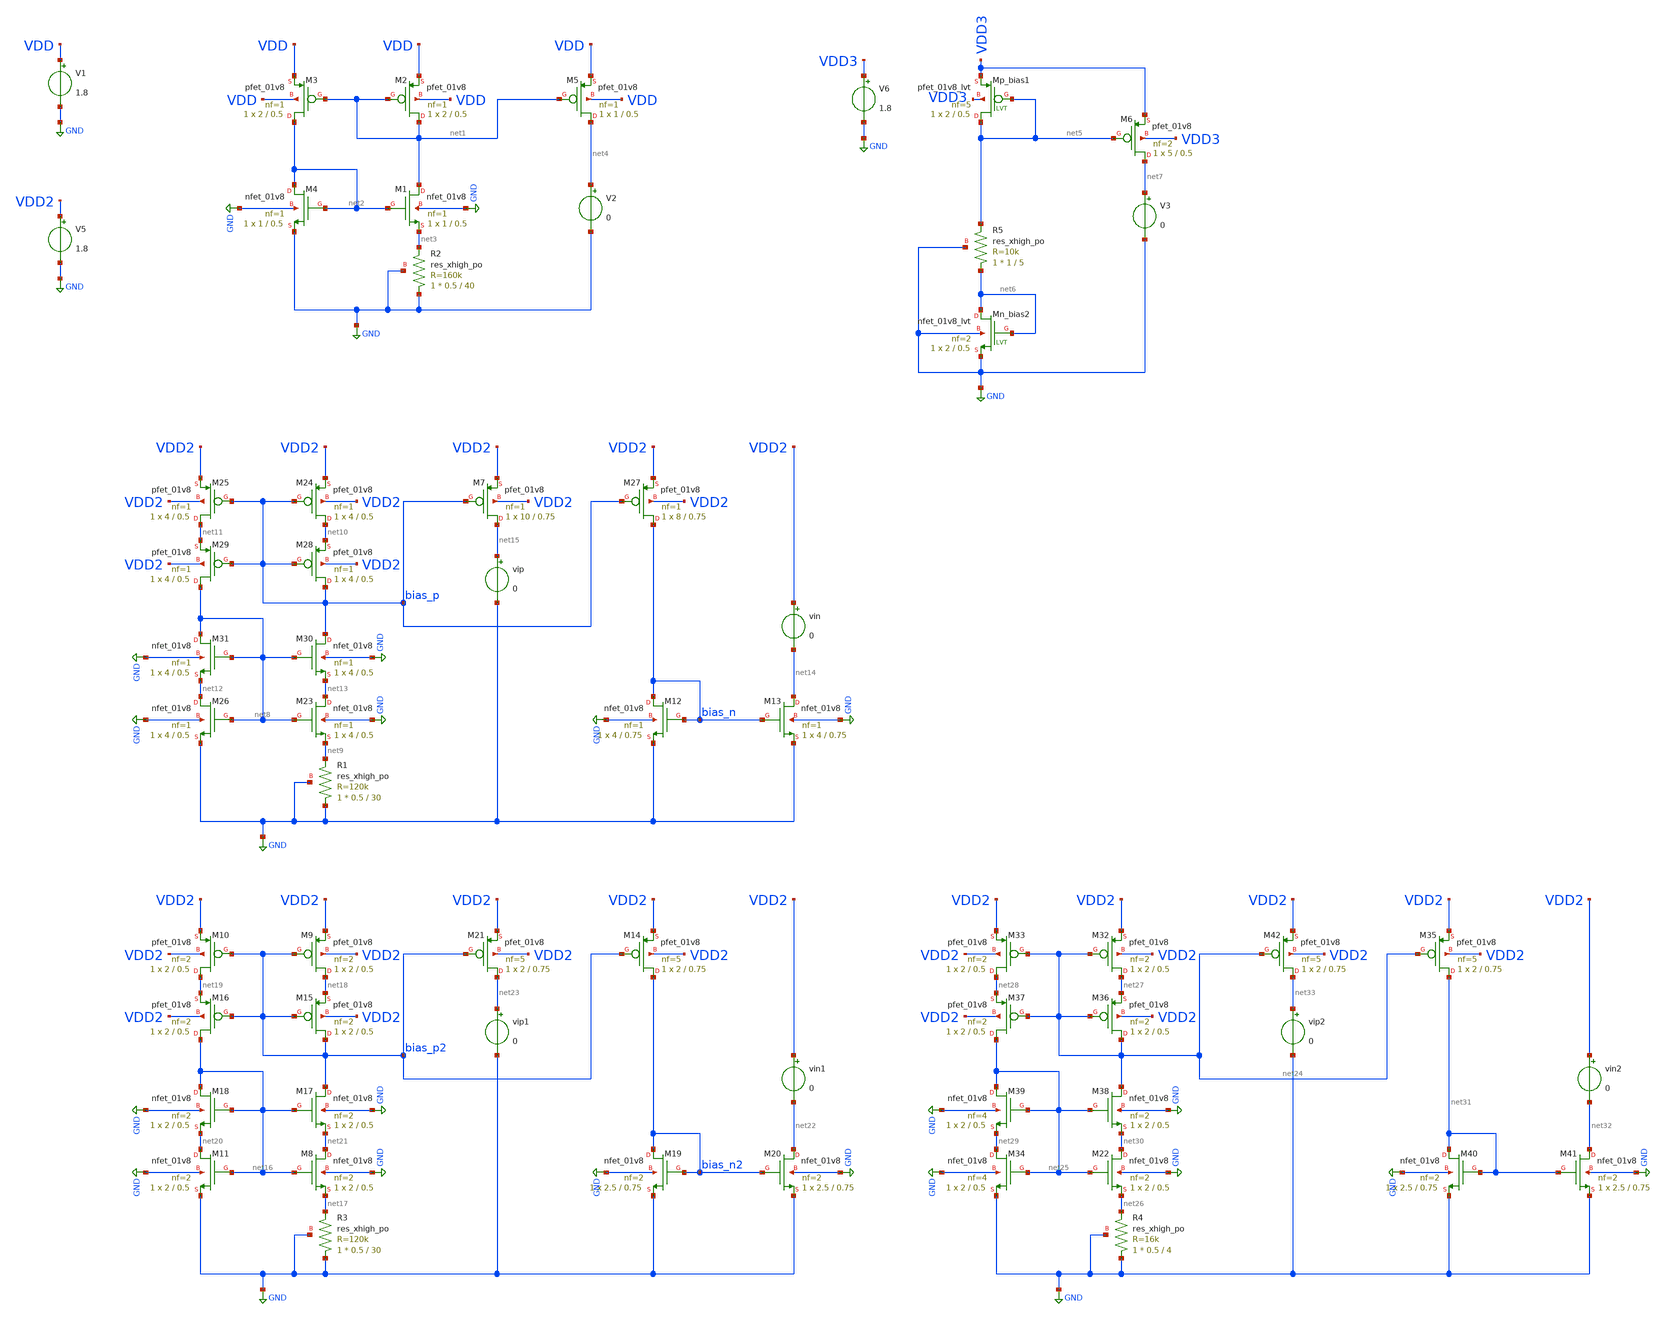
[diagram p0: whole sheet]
** sch_path: schem/ptat_isource.sch
**.subckt ptat_isource
XM1 net1 net2 net3 GND sky130_fd_pr__nfet_01v8 L=0.5 W=1 nf=1 ad='int((1 + 1)/2) * 1 / 1 * 0.29' as='int((1 + 2)/2) * 1 / 1 * 0.29'
+ pd='2*int((1 + 1)/2) * (1 / 1 + 0.29)' ps='2*int((1 + 2)/2) * (1 / 1 + 0.29)' nrd='0.29 / 1 ' nrs='0.29 / 1 '
+ sa=0 sb=0 sd=0 mult=1 m=1
XM2 net1 net1 VDD VDD sky130_fd_pr__pfet_01v8 L=0.5 W=2 nf=1 ad='int((1 + 1)/2) * 2 / 1 * 0.29' as='int((1 + 2)/2) * 2 / 1 * 0.29'
+ pd='2*int((1 + 1)/2) * (2 / 1 + 0.29)' ps='2*int((1 + 2)/2) * (2 / 1 + 0.29)' nrd='0.29 / 2 ' nrs='0.29 / 2 '
+ sa=0 sb=0 sd=0 mult=1 m=1
XM3 net2 net1 VDD VDD sky130_fd_pr__pfet_01v8 L=0.5 W=2 nf=1 ad='int((1 + 1)/2) * 2 / 1 * 0.29' as='int((1 + 2)/2) * 2 / 1 * 0.29'
+ pd='2*int((1 + 1)/2) * (2 / 1 + 0.29)' ps='2*int((1 + 2)/2) * (2 / 1 + 0.29)' nrd='0.29 / 2 ' nrs='0.29 / 2 '
+ sa=0 sb=0 sd=0 mult=1 m=1
XM4 net2 net2 GND GND sky130_fd_pr__nfet_01v8 L=0.5 W=1 nf=1 ad='int((1 + 1)/2) * 1 / 1 * 0.29' as='int((1 + 2)/2) * 1 / 1 * 0.29'
+ pd='2*int((1 + 1)/2) * (1 / 1 + 0.29)' ps='2*int((1 + 2)/2) * (1 / 1 + 0.29)' nrd='0.29 / 1 ' nrs='0.29 / 1 '
+ sa=0 sb=0 sd=0 mult=1 m=1
XR2 GND net3 GND sky130_fd_pr__res_xhigh_po W=0.5 L=40 mult=1 m=1
V1 VDD GND 1.8
XM5 net4 net1 VDD VDD sky130_fd_pr__pfet_01v8 L=0.5 W=1 nf=1 ad='int((1 + 1)/2) * 1 / 1 * 0.29' as='int((1 + 2)/2) * 1 / 1 * 0.29'
+ pd='2*int((1 + 1)/2) * (1 / 1 + 0.29)' ps='2*int((1 + 2)/2) * (1 / 1 + 0.29)' nrd='0.29 / 1 ' nrs='0.29 / 1 '
+ sa=0 sb=0 sd=0 mult=1 m=1
V2 net4 GND 0
XM6 net7 net5 VDD3 VDD3 sky130_fd_pr__pfet_01v8 L=0.5 W=5 nf=2 ad='int((2 + 1)/2) * 5 / 2 * 0.29' as='int((2 + 2)/2) * 5 / 2 * 0.29'
+ pd='2*int((2 + 1)/2) * (5 / 2 + 0.29)' ps='2*int((2 + 2)/2) * (5 / 2 + 0.29)' nrd='0.29 / 5 ' nrs='0.29 / 5 '
+ sa=0 sb=0 sd=0 mult=1 m=1
V3 net7 GND 0
XMn_bias2 net6 net6 GND GND sky130_fd_pr__nfet_01v8_lvt L=0.5 W=2 nf=2 ad='int((nf+1)/2) * W/nf * 0.29'
+ as='int((nf+2)/2) * W/nf * 0.29' pd='2*int((nf+1)/2) * (W/nf + 0.29)' ps='2*int((nf+2)/2) * (W/nf + 0.29)'
+ nrd='0.29 / W' nrs='0.29 / W' sa=0 sb=0 sd=0 mult=1 m=1
XMp_bias1 net5 net5 VDD3 VDD3 sky130_fd_pr__pfet_01v8_lvt L=0.5 W=2 nf=5 ad='int((nf+1)/2) * W/nf * 0.29'
+ as='int((nf+2)/2) * W/nf * 0.29' pd='2*int((nf+1)/2) * (W/nf + 0.29)' ps='2*int((nf+2)/2) * (W/nf + 0.29)'
+ nrd='0.29 / W' nrs='0.29 / W' sa=0 sb=0 sd=0 mult=1 m=1
V5 VDD2 GND 1.8
V6 VDD3 GND 1.8
XM23 net13 net8 net9 GND sky130_fd_pr__nfet_01v8 L=0.5 W=4 nf=1 ad='int((1 + 1)/2) * 4 / 1 * 0.29' as='int((1 + 2)/2) * 4 / 1 * 0.29'
+ pd='2*int((1 + 1)/2) * (4 / 1 + 0.29)' ps='2*int((1 + 2)/2) * (4 / 1 + 0.29)' nrd='0.29 / 4 ' nrs='0.29 / 4 '
+ sa=0 sb=0 sd=0 mult=1 m=1
XM24 net10 bias_p VDD2 VDD2 sky130_fd_pr__pfet_01v8 L=0.5 W=4 nf=1 ad='int((1 + 1)/2) * 4 / 1 * 0.29'
+ as='int((1 + 2)/2) * 4 / 1 * 0.29' pd='2*int((1 + 1)/2) * (4 / 1 + 0.29)' ps='2*int((1 + 2)/2) * (4 / 1 + 0.29)'
+ nrd='0.29 / 4 ' nrs='0.29 / 4 ' sa=0 sb=0 sd=0 mult=1 m=1
XM25 net11 bias_p VDD2 VDD2 sky130_fd_pr__pfet_01v8 L=0.5 W=4 nf=1 ad='int((1 + 1)/2) * 4 / 1 * 0.29'
+ as='int((1 + 2)/2) * 4 / 1 * 0.29' pd='2*int((1 + 1)/2) * (4 / 1 + 0.29)' ps='2*int((1 + 2)/2) * (4 / 1 + 0.29)'
+ nrd='0.29 / 4 ' nrs='0.29 / 4 ' sa=0 sb=0 sd=0 mult=1 m=1
XM26 net12 net8 GND GND sky130_fd_pr__nfet_01v8 L=0.5 W=4 nf=1 ad='int((1 + 1)/2) * 4 / 1 * 0.29' as='int((1 + 2)/2) * 4 / 1 * 0.29'
+ pd='2*int((1 + 1)/2) * (4 / 1 + 0.29)' ps='2*int((1 + 2)/2) * (4 / 1 + 0.29)' nrd='0.29 / 4 ' nrs='0.29 / 4 '
+ sa=0 sb=0 sd=0 mult=1 m=1
XR1 GND net9 GND sky130_fd_pr__res_xhigh_po W=0.5 L=30 mult=1 m=1
XM27 bias_n bias_p VDD2 VDD2 sky130_fd_pr__pfet_01v8 L=0.75 W=8 nf=1 ad='int((1 + 1)/2) * 8 / 1 * 0.29'
+ as='int((1 + 2)/2) * 8 / 1 * 0.29' pd='2*int((1 + 1)/2) * (8 / 1 + 0.29)' ps='2*int((1 + 2)/2) * (8 / 1 + 0.29)'
+ nrd='0.29 / 8 ' nrs='0.29 / 8 ' sa=0 sb=0 sd=0 mult=1 m=1
XM28 bias_p bias_p net10 VDD2 sky130_fd_pr__pfet_01v8 L=0.5 W=4 nf=1 ad='int((1 + 1)/2) * 4 / 1 * 0.29'
+ as='int((1 + 2)/2) * 4 / 1 * 0.29' pd='2*int((1 + 1)/2) * (4 / 1 + 0.29)' ps='2*int((1 + 2)/2) * (4 / 1 + 0.29)'
+ nrd='0.29 / 4 ' nrs='0.29 / 4 ' sa=0 sb=0 sd=0 mult=1 m=1
XM29 net8 bias_p net11 VDD2 sky130_fd_pr__pfet_01v8 L=0.5 W=4 nf=1 ad='int((1 + 1)/2) * 4 / 1 * 0.29'
+ as='int((1 + 2)/2) * 4 / 1 * 0.29' pd='2*int((1 + 1)/2) * (4 / 1 + 0.29)' ps='2*int((1 + 2)/2) * (4 / 1 + 0.29)'
+ nrd='0.29 / 4 ' nrs='0.29 / 4 ' sa=0 sb=0 sd=0 mult=1 m=1
XM30 bias_p net8 net13 GND sky130_fd_pr__nfet_01v8 L=0.5 W=4 nf=1 ad='int((1 + 1)/2) * 4 / 1 * 0.29'
+ as='int((1 + 2)/2) * 4 / 1 * 0.29' pd='2*int((1 + 1)/2) * (4 / 1 + 0.29)' ps='2*int((1 + 2)/2) * (4 / 1 + 0.29)'
+ nrd='0.29 / 4 ' nrs='0.29 / 4 ' sa=0 sb=0 sd=0 mult=1 m=1
XM31 net8 net8 net12 GND sky130_fd_pr__nfet_01v8 L=0.5 W=4 nf=1 ad='int((1 + 1)/2) * 4 / 1 * 0.29' as='int((1 + 2)/2) * 4 / 1 * 0.29'
+ pd='2*int((1 + 1)/2) * (4 / 1 + 0.29)' ps='2*int((1 + 2)/2) * (4 / 1 + 0.29)' nrd='0.29 / 4 ' nrs='0.29 / 4 '
+ sa=0 sb=0 sd=0 mult=1 m=1
XM12 bias_n bias_n GND GND sky130_fd_pr__nfet_01v8 L=0.75 W=4 nf=1 ad='int((1 + 1)/2) * 4 / 1 * 0.29'
+ as='int((1 + 2)/2) * 4 / 1 * 0.29' pd='2*int((1 + 1)/2) * (4 / 1 + 0.29)' ps='2*int((1 + 2)/2) * (4 / 1 + 0.29)'
+ nrd='0.29 / 4 ' nrs='0.29 / 4 ' sa=0 sb=0 sd=0 mult=1 m=1
XM13 net14 bias_n GND GND sky130_fd_pr__nfet_01v8 L=0.75 W=4 nf=1 ad='int((1 + 1)/2) * 4 / 1 * 0.29'
+ as='int((1 + 2)/2) * 4 / 1 * 0.29' pd='2*int((1 + 1)/2) * (4 / 1 + 0.29)' ps='2*int((1 + 2)/2) * (4 / 1 + 0.29)'
+ nrd='0.29 / 4 ' nrs='0.29 / 4 ' sa=0 sb=0 sd=0 mult=1 m=1
vin VDD2 net14 0
XM7 net15 bias_p VDD2 VDD2 sky130_fd_pr__pfet_01v8 L=0.75 W=10 nf=1 ad='int((1 + 1)/2) * 10 / 1 * 0.29'
+ as='int((1 + 2)/2) * 10 / 1 * 0.29' pd='2*int((1 + 1)/2) * (10 / 1 + 0.29)' ps='2*int((1 + 2)/2) * (10 / 1 + 0.29)'
+ nrd='0.29 / 10 ' nrs='0.29 / 10 ' sa=0 sb=0 sd=0 mult=1 m=1
vip net15 GND 0
XM8 net21 net16 net17 GND sky130_fd_pr__nfet_01v8 L=0.5 W=2 nf=2 ad='int((2 + 1)/2) * 2 / 2 * 0.29' as='int((2 + 2)/2) * 2 / 2 * 0.29'
+ pd='2*int((2 + 1)/2) * (2 / 2 + 0.29)' ps='2*int((2 + 2)/2) * (2 / 2 + 0.29)' nrd='0.29 / 2 ' nrs='0.29 / 2 '
+ sa=0 sb=0 sd=0 mult=1 m=1
XM9 net18 bias_p2 VDD2 VDD2 sky130_fd_pr__pfet_01v8 L=0.5 W=2 nf=2 ad='int((2 + 1)/2) * 2 / 2 * 0.29'
+ as='int((2 + 2)/2) * 2 / 2 * 0.29' pd='2*int((2 + 1)/2) * (2 / 2 + 0.29)' ps='2*int((2 + 2)/2) * (2 / 2 + 0.29)'
+ nrd='0.29 / 2 ' nrs='0.29 / 2 ' sa=0 sb=0 sd=0 mult=1 m=1
XM10 net19 bias_p2 VDD2 VDD2 sky130_fd_pr__pfet_01v8 L=0.5 W=2 nf=2 ad='int((2 + 1)/2) * 2 / 2 * 0.29'
+ as='int((2 + 2)/2) * 2 / 2 * 0.29' pd='2*int((2 + 1)/2) * (2 / 2 + 0.29)' ps='2*int((2 + 2)/2) * (2 / 2 + 0.29)'
+ nrd='0.29 / 2 ' nrs='0.29 / 2 ' sa=0 sb=0 sd=0 mult=1 m=1
XM11 net20 net16 GND GND sky130_fd_pr__nfet_01v8 L=0.5 W=2 nf=2 ad='int((2 + 1)/2) * 2 / 2 * 0.29' as='int((2 + 2)/2) * 2 / 2 * 0.29'
+ pd='2*int((2 + 1)/2) * (2 / 2 + 0.29)' ps='2*int((2 + 2)/2) * (2 / 2 + 0.29)' nrd='0.29 / 2 ' nrs='0.29 / 2 '
+ sa=0 sb=0 sd=0 mult=1 m=1
XR3 GND net17 GND sky130_fd_pr__res_xhigh_po W=0.5 L=30 mult=1 m=1
XM14 bias_n2 bias_p2 VDD2 VDD2 sky130_fd_pr__pfet_01v8 L=0.75 W=2 nf=5 ad='int((5 + 1)/2) * 2 / 5 * 0.29'
+ as='int((5 + 2)/2) * 2 / 5 * 0.29' pd='2*int((5 + 1)/2) * (2 / 5 + 0.29)' ps='2*int((5 + 2)/2) * (2 / 5 + 0.29)'
+ nrd='0.29 / 2 ' nrs='0.29 / 2 ' sa=0 sb=0 sd=0 mult=1 m=1
XM15 bias_p2 bias_p2 net18 VDD2 sky130_fd_pr__pfet_01v8 L=0.5 W=2 nf=2 ad='int((2 + 1)/2) * 2 / 2 * 0.29'
+ as='int((2 + 2)/2) * 2 / 2 * 0.29' pd='2*int((2 + 1)/2) * (2 / 2 + 0.29)' ps='2*int((2 + 2)/2) * (2 / 2 + 0.29)'
+ nrd='0.29 / 2 ' nrs='0.29 / 2 ' sa=0 sb=0 sd=0 mult=1 m=1
XM16 net16 bias_p2 net19 VDD2 sky130_fd_pr__pfet_01v8 L=0.5 W=2 nf=2 ad='int((2 + 1)/2) * 2 / 2 * 0.29'
+ as='int((2 + 2)/2) * 2 / 2 * 0.29' pd='2*int((2 + 1)/2) * (2 / 2 + 0.29)' ps='2*int((2 + 2)/2) * (2 / 2 + 0.29)'
+ nrd='0.29 / 2 ' nrs='0.29 / 2 ' sa=0 sb=0 sd=0 mult=1 m=1
XM17 bias_p2 net16 net21 GND sky130_fd_pr__nfet_01v8 L=0.5 W=2 nf=2 ad='int((2 + 1)/2) * 2 / 2 * 0.29'
+ as='int((2 + 2)/2) * 2 / 2 * 0.29' pd='2*int((2 + 1)/2) * (2 / 2 + 0.29)' ps='2*int((2 + 2)/2) * (2 / 2 + 0.29)'
+ nrd='0.29 / 2 ' nrs='0.29 / 2 ' sa=0 sb=0 sd=0 mult=1 m=1
XM18 net16 net16 net20 GND sky130_fd_pr__nfet_01v8 L=0.5 W=2 nf=2 ad='int((2 + 1)/2) * 2 / 2 * 0.29'
+ as='int((2 + 2)/2) * 2 / 2 * 0.29' pd='2*int((2 + 1)/2) * (2 / 2 + 0.29)' ps='2*int((2 + 2)/2) * (2 / 2 + 0.29)'
+ nrd='0.29 / 2 ' nrs='0.29 / 2 ' sa=0 sb=0 sd=0 mult=1 m=1
XM19 bias_n2 bias_n2 GND GND sky130_fd_pr__nfet_01v8 L=0.75 W=2.5 nf=2 ad='int((2 + 1)/2) * 2.5 / 2 * 0.29'
+ as='int((2 + 2)/2) * 2.5 / 2 * 0.29' pd='2*int((2 + 1)/2) * (2.5 / 2 + 0.29)' ps='2*int((2 + 2)/2) * (2.5 / 2 + 0.29)'
+ nrd='0.29 / 2.5 ' nrs='0.29 / 2.5 ' sa=0 sb=0 sd=0 mult=1 m=1
XM20 net22 bias_n2 GND GND sky130_fd_pr__nfet_01v8 L=0.75 W=2.5 nf=2 ad='int((2 + 1)/2) * 2.5 / 2 * 0.29'
+ as='int((2 + 2)/2) * 2.5 / 2 * 0.29' pd='2*int((2 + 1)/2) * (2.5 / 2 + 0.29)' ps='2*int((2 + 2)/2) * (2.5 / 2 + 0.29)'
+ nrd='0.29 / 2.5 ' nrs='0.29 / 2.5 ' sa=0 sb=0 sd=0 mult=1 m=1
vin1 VDD2 net22 0
XM21 net23 bias_p2 VDD2 VDD2 sky130_fd_pr__pfet_01v8 L=0.75 W=2 nf=5 ad='int((5 + 1)/2) * 2 / 5 * 0.29'
+ as='int((5 + 2)/2) * 2 / 5 * 0.29' pd='2*int((5 + 1)/2) * (2 / 5 + 0.29)' ps='2*int((5 + 2)/2) * (2 / 5 + 0.29)'
+ nrd='0.29 / 2 ' nrs='0.29 / 2 ' sa=0 sb=0 sd=0 mult=1 m=1
vip1 net23 GND 0
XM22 net30 net25 net26 GND sky130_fd_pr__nfet_01v8 L=0.5 W=2 nf=2 ad='int((2 + 1)/2) * 2 / 2 * 0.29'
+ as='int((2 + 2)/2) * 2 / 2 * 0.29' pd='2*int((2 + 1)/2) * (2 / 2 + 0.29)' ps='2*int((2 + 2)/2) * (2 / 2 + 0.29)'
+ nrd='0.29 / 2 ' nrs='0.29 / 2 ' sa=0 sb=0 sd=0 mult=1 m=1
XM32 net27 net24 VDD2 VDD2 sky130_fd_pr__pfet_01v8 L=0.5 W=2 nf=2 ad='int((2 + 1)/2) * 2 / 2 * 0.29'
+ as='int((2 + 2)/2) * 2 / 2 * 0.29' pd='2*int((2 + 1)/2) * (2 / 2 + 0.29)' ps='2*int((2 + 2)/2) * (2 / 2 + 0.29)'
+ nrd='0.29 / 2 ' nrs='0.29 / 2 ' sa=0 sb=0 sd=0 mult=1 m=1
XM33 net28 net24 VDD2 VDD2 sky130_fd_pr__pfet_01v8 L=0.5 W=2 nf=2 ad='int((2 + 1)/2) * 2 / 2 * 0.29'
+ as='int((2 + 2)/2) * 2 / 2 * 0.29' pd='2*int((2 + 1)/2) * (2 / 2 + 0.29)' ps='2*int((2 + 2)/2) * (2 / 2 + 0.29)'
+ nrd='0.29 / 2 ' nrs='0.29 / 2 ' sa=0 sb=0 sd=0 mult=1 m=1
XM34 net29 net25 GND GND sky130_fd_pr__nfet_01v8 L=0.5 W=2 nf=4 ad='int((4 + 1)/2) * 2 / 4 * 0.29' as='int((4 + 2)/2) * 2 / 4 * 0.29'
+ pd='2*int((4 + 1)/2) * (2 / 4 + 0.29)' ps='2*int((4 + 2)/2) * (2 / 4 + 0.29)' nrd='0.29 / 2 ' nrs='0.29 / 2 '
+ sa=0 sb=0 sd=0 mult=1 m=1
XR4 GND net26 GND sky130_fd_pr__res_xhigh_po W=0.5 L=4 mult=1 m=1
XM35 net31 net24 VDD2 VDD2 sky130_fd_pr__pfet_01v8 L=0.75 W=2 nf=5 ad='int((5 + 1)/2) * 2 / 5 * 0.29'
+ as='int((5 + 2)/2) * 2 / 5 * 0.29' pd='2*int((5 + 1)/2) * (2 / 5 + 0.29)' ps='2*int((5 + 2)/2) * (2 / 5 + 0.29)'
+ nrd='0.29 / 2 ' nrs='0.29 / 2 ' sa=0 sb=0 sd=0 mult=1 m=1
XM36 net24 net24 net27 VDD2 sky130_fd_pr__pfet_01v8 L=0.5 W=2 nf=2 ad='int((2 + 1)/2) * 2 / 2 * 0.29'
+ as='int((2 + 2)/2) * 2 / 2 * 0.29' pd='2*int((2 + 1)/2) * (2 / 2 + 0.29)' ps='2*int((2 + 2)/2) * (2 / 2 + 0.29)'
+ nrd='0.29 / 2 ' nrs='0.29 / 2 ' sa=0 sb=0 sd=0 mult=1 m=1
XM37 net25 net24 net28 VDD2 sky130_fd_pr__pfet_01v8 L=0.5 W=2 nf=2 ad='int((2 + 1)/2) * 2 / 2 * 0.29'
+ as='int((2 + 2)/2) * 2 / 2 * 0.29' pd='2*int((2 + 1)/2) * (2 / 2 + 0.29)' ps='2*int((2 + 2)/2) * (2 / 2 + 0.29)'
+ nrd='0.29 / 2 ' nrs='0.29 / 2 ' sa=0 sb=0 sd=0 mult=1 m=1
XM38 net24 net25 net30 GND sky130_fd_pr__nfet_01v8 L=0.5 W=2 nf=2 ad='int((2 + 1)/2) * 2 / 2 * 0.29'
+ as='int((2 + 2)/2) * 2 / 2 * 0.29' pd='2*int((2 + 1)/2) * (2 / 2 + 0.29)' ps='2*int((2 + 2)/2) * (2 / 2 + 0.29)'
+ nrd='0.29 / 2 ' nrs='0.29 / 2 ' sa=0 sb=0 sd=0 mult=1 m=1
XM39 net25 net25 net29 GND sky130_fd_pr__nfet_01v8 L=0.5 W=2 nf=4 ad='int((4 + 1)/2) * 2 / 4 * 0.29'
+ as='int((4 + 2)/2) * 2 / 4 * 0.29' pd='2*int((4 + 1)/2) * (2 / 4 + 0.29)' ps='2*int((4 + 2)/2) * (2 / 4 + 0.29)'
+ nrd='0.29 / 2 ' nrs='0.29 / 2 ' sa=0 sb=0 sd=0 mult=1 m=1
XM40 net31 net31 GND GND sky130_fd_pr__nfet_01v8 L=0.75 W=2.5 nf=2 ad='int((2 + 1)/2) * 2.5 / 2 * 0.29'
+ as='int((2 + 2)/2) * 2.5 / 2 * 0.29' pd='2*int((2 + 1)/2) * (2.5 / 2 + 0.29)' ps='2*int((2 + 2)/2) * (2.5 / 2 + 0.29)'
+ nrd='0.29 / 2.5 ' nrs='0.29 / 2.5 ' sa=0 sb=0 sd=0 mult=1 m=1
XM41 net32 net31 GND GND sky130_fd_pr__nfet_01v8 L=0.75 W=2.5 nf=2 ad='int((2 + 1)/2) * 2.5 / 2 * 0.29'
+ as='int((2 + 2)/2) * 2.5 / 2 * 0.29' pd='2*int((2 + 1)/2) * (2.5 / 2 + 0.29)' ps='2*int((2 + 2)/2) * (2.5 / 2 + 0.29)'
+ nrd='0.29 / 2.5 ' nrs='0.29 / 2.5 ' sa=0 sb=0 sd=0 mult=1 m=1
vin2 VDD2 net32 0
XM42 net33 net24 VDD2 VDD2 sky130_fd_pr__pfet_01v8 L=0.75 W=2 nf=5 ad='int((5 + 1)/2) * 2 / 5 * 0.29'
+ as='int((5 + 2)/2) * 2 / 5 * 0.29' pd='2*int((5 + 1)/2) * (2 / 5 + 0.29)' ps='2*int((5 + 2)/2) * (2 / 5 + 0.29)'
+ nrd='0.29 / 2 ' nrs='0.29 / 2 ' sa=0 sb=0 sd=0 mult=1 m=1
vip2 net33 GND 0
XR5 net6 net5 GND sky130_fd_pr__res_xhigh_po W=1 L=5 mult=1 m=1
**** begin user architecture code


.lib /usr/local/share/pdk/sky130A/libs.tech/ngspice/sky130.lib.spice ff

.op
.save all

.control
  set noaskquit

  let n = 7
  let tvec = vector(n)

  let ivec = vector(n)
  let ivec2p = vector(n)
  let ivec2n = vector(n)
  let ivec3p = vector(n)
  let ivec3n = vector(n)
  let ivec4p = vector(n)
  let ivec4n = vector(n)

  let refvec = vector(n)
  let idx = 0

  foreach t -40 -20 0 27 60 85 125
    set temp = $t
    run

    let tvec[idx] = $t

    let ivec[idx] = i(v2)
    let ivec2p[idx] = i(vip)
    let ivec2n[idx] = i(vin)
    let ivec3p[idx] = i(vip1)
    let ivec3n[idx] = i(vin1)
    let ivec4p[idx] = i(vip2)
    let ivec4n[idx] = i(vin2)

    let refvec[idx] = i(v3)

    print $t i(v2)
    print $t i(v3)

    let idx = idx + 1
  end

  plot ivec4p ivec4n refvec vs tvec

.endc

.end


**** end user architecture code
**.ends
.GLOBAL GND
.end
